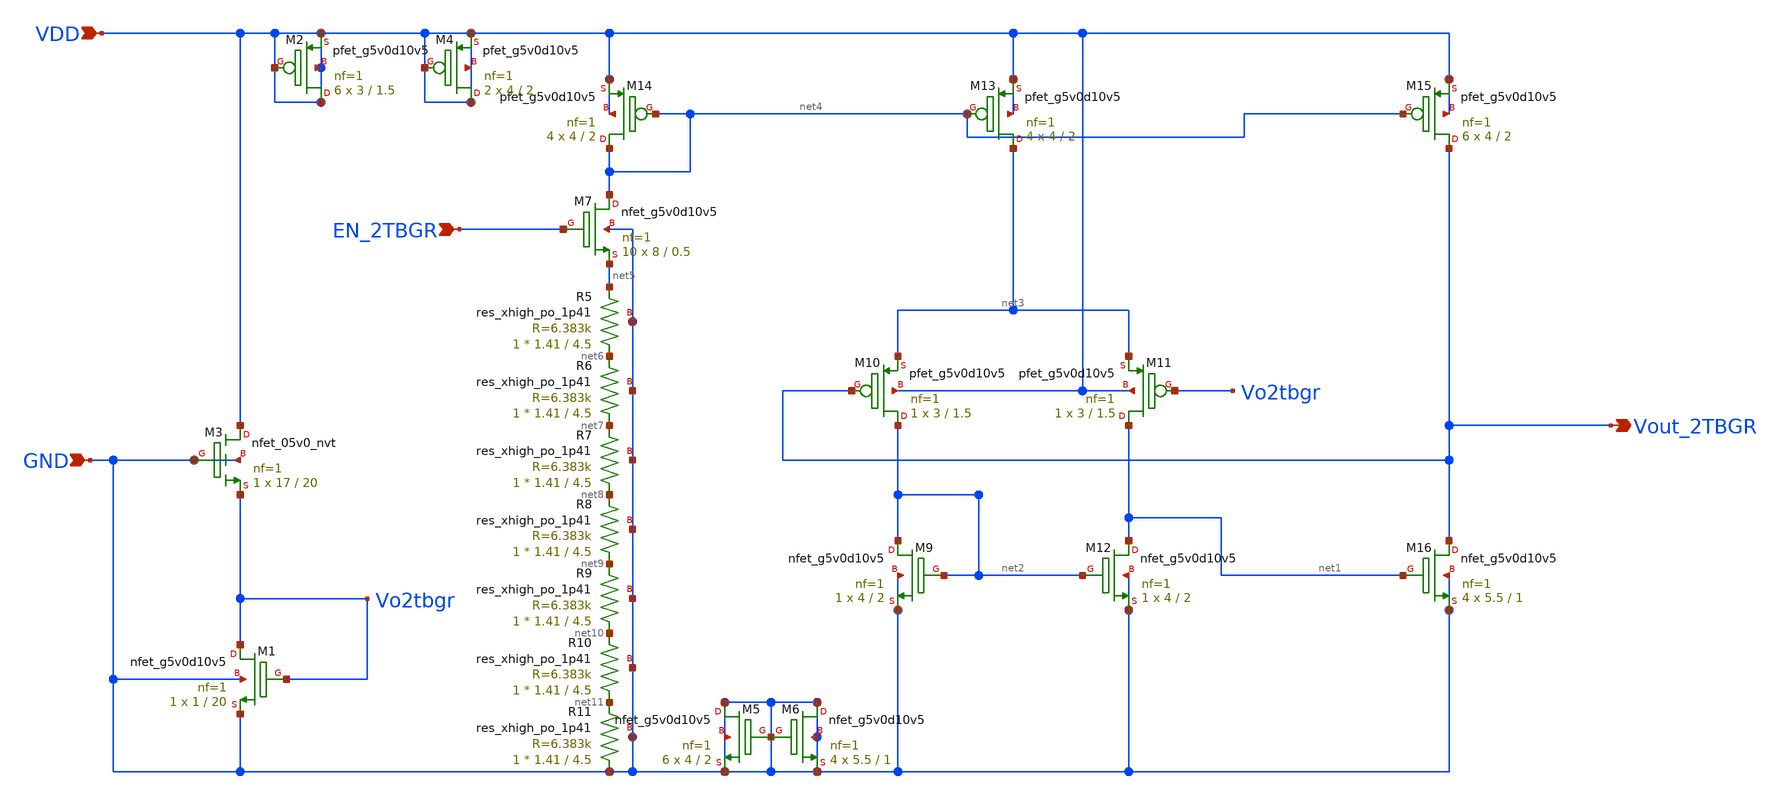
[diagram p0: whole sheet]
** sch_path: 2TBGR/Schematics/Twotran-BGR.sch
**.subckt Twotran-BGR GND VDD Vout_2TBGR EN_2TBGR
*.ipin GND
*.ipin VDD
*.opin Vout_2TBGR
*.ipin EN_2TBGR
XM3 VDD GND Vo2tbgr GND sky130_fd_pr__nfet_05v0_nvt L=20 W=17 nf=1 ad='int((nf+1)/2) * W/nf * 0.29' as='int((nf+2)/2) * W/nf * 0.29'
+ pd='2*int((nf+1)/2) * (W/nf + 0.29)' ps='2*int((nf+2)/2) * (W/nf + 0.29)' nrd='0.29 / W' nrs='0.29 / W'
+ sa=0 sb=0 sd=0 mult=1 m=1
XM1 Vo2tbgr Vo2tbgr GND GND sky130_fd_pr__nfet_g5v0d10v5 L=20 W=1 nf=1 ad='int((nf+1)/2) * W/nf * 0.29'
+ as='int((nf+2)/2) * W/nf * 0.29' pd='2*int((nf+1)/2) * (W/nf + 0.29)' ps='2*int((nf+2)/2) * (W/nf + 0.29)'
+ nrd='0.29 / W' nrs='0.29 / W' sa=0 sb=0 sd=0 mult=1 m=1
XM9 net2 net2 GND GND sky130_fd_pr__nfet_g5v0d10v5 L=2 W=4 nf=1 ad='int((nf+1)/2) * W/nf * 0.29' as='int((nf+2)/2) * W/nf * 0.29'
+ pd='2*int((nf+1)/2) * (W/nf + 0.29)' ps='2*int((nf+2)/2) * (W/nf + 0.29)' nrd='0.29 / W' nrs='0.29 / W'
+ sa=0 sb=0 sd=0 mult=1 m=1
XM10 net2 Vout_2TBGR net3 VDD sky130_fd_pr__pfet_g5v0d10v5 L=1.5 W=3 nf=1 ad='int((nf+1)/2) * W/nf * 0.29'
+ as='int((nf+2)/2) * W/nf * 0.29' pd='2*int((nf+1)/2) * (W/nf + 0.29)' ps='2*int((nf+2)/2) * (W/nf + 0.29)'
+ nrd='0.29 / W' nrs='0.29 / W' sa=0 sb=0 sd=0 mult=1 m=1
XM11 net1 Vo2tbgr net3 VDD sky130_fd_pr__pfet_g5v0d10v5 L=1.5 W=3 nf=1 ad='int((nf+1)/2) * W/nf * 0.29'
+ as='int((nf+2)/2) * W/nf * 0.29' pd='2*int((nf+1)/2) * (W/nf + 0.29)' ps='2*int((nf+2)/2) * (W/nf + 0.29)'
+ nrd='0.29 / W' nrs='0.29 / W' sa=0 sb=0 sd=0 mult=1 m=1
XM12 net1 net2 GND GND sky130_fd_pr__nfet_g5v0d10v5 L=2 W=4 nf=1 ad='int((nf+1)/2) * W/nf * 0.29' as='int((nf+2)/2) * W/nf * 0.29'
+ pd='2*int((nf+1)/2) * (W/nf + 0.29)' ps='2*int((nf+2)/2) * (W/nf + 0.29)' nrd='0.29 / W' nrs='0.29 / W'
+ sa=0 sb=0 sd=0 mult=1 m=1
XM13 net3 net4 VDD VDD sky130_fd_pr__pfet_g5v0d10v5 L=2 W=4 nf=1 ad='int((nf+1)/2) * W/nf * 0.29' as='int((nf+2)/2) * W/nf * 0.29'
+ pd='2*int((nf+1)/2) * (W/nf + 0.29)' ps='2*int((nf+2)/2) * (W/nf + 0.29)' nrd='0.29 / W' nrs='0.29 / W'
+ sa=0 sb=0 sd=0 mult=4 m=4
XM14 net4 net4 VDD VDD sky130_fd_pr__pfet_g5v0d10v5 L=2 W=4 nf=1 ad='int((nf+1)/2) * W/nf * 0.29' as='int((nf+2)/2) * W/nf * 0.29'
+ pd='2*int((nf+1)/2) * (W/nf + 0.29)' ps='2*int((nf+2)/2) * (W/nf + 0.29)' nrd='0.29 / W' nrs='0.29 / W'
+ sa=0 sb=0 sd=0 mult=4 m=4
XM15 Vout_2TBGR net4 VDD VDD sky130_fd_pr__pfet_g5v0d10v5 L=2 W=4 nf=1 ad='int((nf+1)/2) * W/nf * 0.29'
+ as='int((nf+2)/2) * W/nf * 0.29' pd='2*int((nf+1)/2) * (W/nf + 0.29)' ps='2*int((nf+2)/2) * (W/nf + 0.29)'
+ nrd='0.29 / W' nrs='0.29 / W' sa=0 sb=0 sd=0 mult=6 m=6
XM16 Vout_2TBGR net1 GND GND sky130_fd_pr__nfet_g5v0d10v5 L=1 W=5.5 nf=1 ad='int((nf+1)/2) * W/nf * 0.29'
+ as='int((nf+2)/2) * W/nf * 0.29' pd='2*int((nf+1)/2) * (W/nf + 0.29)' ps='2*int((nf+2)/2) * (W/nf + 0.29)'
+ nrd='0.29 / W' nrs='0.29 / W' sa=0 sb=0 sd=0 mult=4 m=4
XR5 net6 net5 GND sky130_fd_pr__res_xhigh_po_1p41 L=4.5 mult=1 m=1
XR6 net7 net6 GND sky130_fd_pr__res_xhigh_po_1p41 L=4.5 mult=1 m=1
XR7 net8 net7 GND sky130_fd_pr__res_xhigh_po_1p41 L=4.5 mult=1 m=1
XR8 net9 net8 GND sky130_fd_pr__res_xhigh_po_1p41 L=4.5 mult=1 m=1
XR9 net10 net9 GND sky130_fd_pr__res_xhigh_po_1p41 L=4.5 mult=1 m=1
XR10 net11 net10 GND sky130_fd_pr__res_xhigh_po_1p41 L=4.5 mult=1 m=1
XR11 GND net11 GND sky130_fd_pr__res_xhigh_po_1p41 L=4.5 mult=1 m=1
XM2 VDD VDD VDD VDD sky130_fd_pr__pfet_g5v0d10v5 L=1.5 W=3 nf=1 ad='int((nf+1)/2) * W/nf * 0.29' as='int((nf+2)/2) * W/nf * 0.29'
+ pd='2*int((nf+1)/2) * (W/nf + 0.29)' ps='2*int((nf+2)/2) * (W/nf + 0.29)' nrd='0.29 / W' nrs='0.29 / W'
+ sa=0 sb=0 sd=0 mult=6 m=6
XM4 VDD VDD VDD VDD sky130_fd_pr__pfet_g5v0d10v5 L=2 W=4 nf=1 ad='int((nf+1)/2) * W/nf * 0.29' as='int((nf+2)/2) * W/nf * 0.29'
+ pd='2*int((nf+1)/2) * (W/nf + 0.29)' ps='2*int((nf+2)/2) * (W/nf + 0.29)' nrd='0.29 / W' nrs='0.29 / W'
+ sa=0 sb=0 sd=0 mult=2 m=2
XM5 GND GND GND GND sky130_fd_pr__nfet_g5v0d10v5 L=2 W=4 nf=1 ad='int((nf+1)/2) * W/nf * 0.29' as='int((nf+2)/2) * W/nf * 0.29'
+ pd='2*int((nf+1)/2) * (W/nf + 0.29)' ps='2*int((nf+2)/2) * (W/nf + 0.29)' nrd='0.29 / W' nrs='0.29 / W'
+ sa=0 sb=0 sd=0 mult=6 m=6
XM6 GND GND GND GND sky130_fd_pr__nfet_g5v0d10v5 L=1 W=5.5 nf=1 ad='int((nf+1)/2) * W/nf * 0.29' as='int((nf+2)/2) * W/nf * 0.29'
+ pd='2*int((nf+1)/2) * (W/nf + 0.29)' ps='2*int((nf+2)/2) * (W/nf + 0.29)' nrd='0.29 / W' nrs='0.29 / W'
+ sa=0 sb=0 sd=0 mult=4 m=4
XM7 net4 EN_2TBGR net5 GND sky130_fd_pr__nfet_g5v0d10v5 L=0.5 W=8 nf=1 ad='int((nf+1)/2) * W/nf * 0.29'
+ as='int((nf+2)/2) * W/nf * 0.29' pd='2*int((nf+1)/2) * (W/nf + 0.29)' ps='2*int((nf+2)/2) * (W/nf + 0.29)'
+ nrd='0.29 / W' nrs='0.29 / W' sa=0 sb=0 sd=0 mult=10 m=10
**.ends
.end
